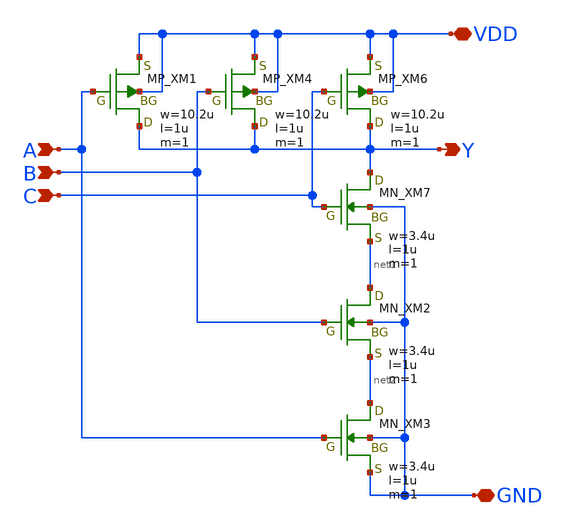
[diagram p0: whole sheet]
** sch_path: openIP62_rev1.0/IP62/Technology/tech/symbols/Xschem/IP62_5_stdcell/NAND3.sch
**.subckt NAND3 B A Y GND VDD C
*.ipin B
*.ipin A
*.opin Y
*.iopin GND
*.iopin VDD
*.ipin C
XM1 Y A VDD VDD PMOS w=10.2u l=1u as=0 ad=0 ps=0 pd=0 nrd=0 nrs=0 m=1
XM4 Y B VDD VDD PMOS w=10.2u l=1u as=0 ad=0 ps=0 pd=0 nrd=0 nrs=0 m=1
XM6 Y C VDD VDD PMOS w=10.2u l=1u as=0 ad=0 ps=0 pd=0 nrd=0 nrs=0 m=1
XM7 Y C net1 GND NMOS w=3.4u l=1u as=0 ad=0 ps=0 pd=0 nrd=0 nrs=0 m=1
XM2 net1 B net2 GND NMOS w=3.4u l=1u as=0 ad=0 ps=0 pd=0 nrd=0 nrs=0 m=1
XM3 net2 A GND GND NMOS w=3.4u l=1u as=0 ad=0 ps=0 pd=0 nrd=0 nrs=0 m=1
**.ends
.end
